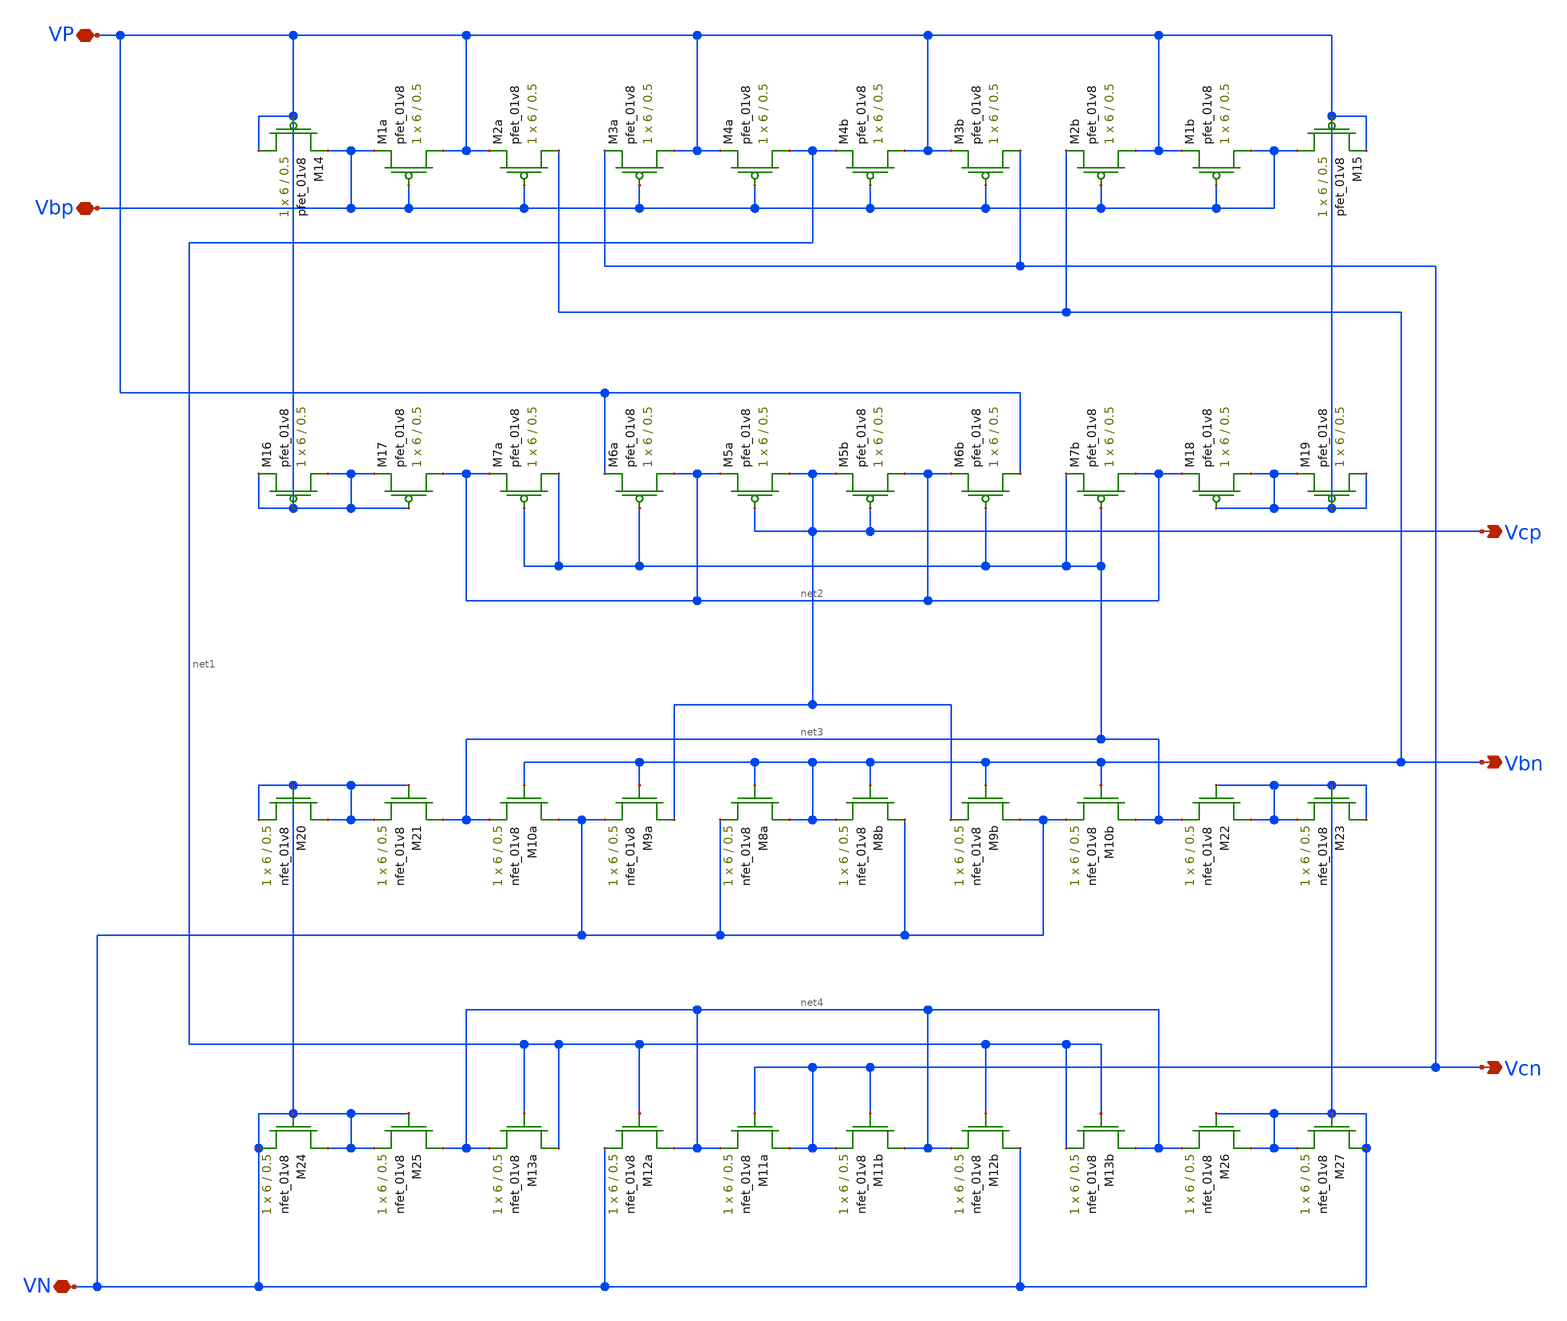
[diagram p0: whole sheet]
** sch_path: schematic/cascode_bias_LDS_old.sch
**.subckt cascode_bias_LDS_old VP VN Vcp Vbn Vcn Vbp
*.iopin VP
*.iopin VN
*.opin Vcp
*.opin Vbn
*.opin Vcn
*.iopin Vbp
XM1a VP Vbp Vbp VDD sky130_fd_pr__pfet_01v8 L=0.5 W=6 nf=1 ad='int((nf+1)/2) * W/nf * 0.29' as='int((nf+2)/2) * W/nf * 0.29'
+ pd='2*int((nf+1)/2) * (W/nf + 0.29)' ps='2*int((nf+2)/2) * (W/nf + 0.29)' nrd='0.29 / W' nrs='0.29 / W'
+ sa=0 sb=0 sd=0 mult=1 m=1
XM2a Vbn Vbp VP VDD sky130_fd_pr__pfet_01v8 L=0.5 W=6 nf=1 ad='int((nf+1)/2) * W/nf * 0.29' as='int((nf+2)/2) * W/nf * 0.29'
+ pd='2*int((nf+1)/2) * (W/nf + 0.29)' ps='2*int((nf+2)/2) * (W/nf + 0.29)' nrd='0.29 / W' nrs='0.29 / W'
+ sa=0 sb=0 sd=0 mult=1 m=1
XM3a VP Vbp Vcn VDD sky130_fd_pr__pfet_01v8 L=0.5 W=6 nf=1 ad='int((nf+1)/2) * W/nf * 0.29' as='int((nf+2)/2) * W/nf * 0.29'
+ pd='2*int((nf+1)/2) * (W/nf + 0.29)' ps='2*int((nf+2)/2) * (W/nf + 0.29)' nrd='0.29 / W' nrs='0.29 / W'
+ sa=0 sb=0 sd=0 mult=1 m=1
XM4a net1 Vbp VP VDD sky130_fd_pr__pfet_01v8 L=0.5 W=6 nf=1 ad='int((nf+1)/2) * W/nf * 0.29' as='int((nf+2)/2) * W/nf * 0.29'
+ pd='2*int((nf+1)/2) * (W/nf + 0.29)' ps='2*int((nf+2)/2) * (W/nf + 0.29)' nrd='0.29 / W' nrs='0.29 / W'
+ sa=0 sb=0 sd=0 mult=1 m=1
XM4b VP Vbp net1 VDD sky130_fd_pr__pfet_01v8 L=0.5 W=6 nf=1 ad='int((nf+1)/2) * W/nf * 0.29' as='int((nf+2)/2) * W/nf * 0.29'
+ pd='2*int((nf+1)/2) * (W/nf + 0.29)' ps='2*int((nf+2)/2) * (W/nf + 0.29)' nrd='0.29 / W' nrs='0.29 / W'
+ sa=0 sb=0 sd=0 mult=1 m=1
XM3b Vcn Vbp VP VDD sky130_fd_pr__pfet_01v8 L=0.5 W=6 nf=1 ad='int((nf+1)/2) * W/nf * 0.29' as='int((nf+2)/2) * W/nf * 0.29'
+ pd='2*int((nf+1)/2) * (W/nf + 0.29)' ps='2*int((nf+2)/2) * (W/nf + 0.29)' nrd='0.29 / W' nrs='0.29 / W'
+ sa=0 sb=0 sd=0 mult=1 m=1
XM2b VP Vbp Vbn VDD sky130_fd_pr__pfet_01v8 L=0.5 W=6 nf=1 ad='int((nf+1)/2) * W/nf * 0.29' as='int((nf+2)/2) * W/nf * 0.29'
+ pd='2*int((nf+1)/2) * (W/nf + 0.29)' ps='2*int((nf+2)/2) * (W/nf + 0.29)' nrd='0.29 / W' nrs='0.29 / W'
+ sa=0 sb=0 sd=0 mult=1 m=1
XM1b Vbp Vbp VP VDD sky130_fd_pr__pfet_01v8 L=0.5 W=6 nf=1 ad='int((nf+1)/2) * W/nf * 0.29' as='int((nf+2)/2) * W/nf * 0.29'
+ pd='2*int((nf+1)/2) * (W/nf + 0.29)' ps='2*int((nf+2)/2) * (W/nf + 0.29)' nrd='0.29 / W' nrs='0.29 / W'
+ sa=0 sb=0 sd=0 mult=1 m=1
XM7a net3 net3 net2 VDD sky130_fd_pr__pfet_01v8 L=0.5 W=6 nf=1 ad='int((nf+1)/2) * W/nf * 0.29' as='int((nf+2)/2) * W/nf * 0.29'
+ pd='2*int((nf+1)/2) * (W/nf + 0.29)' ps='2*int((nf+2)/2) * (W/nf + 0.29)' nrd='0.29 / W' nrs='0.29 / W'
+ sa=0 sb=0 sd=0 mult=1 m=1
XM6a net2 net3 VP VDD sky130_fd_pr__pfet_01v8 L=0.5 W=6 nf=1 ad='int((nf+1)/2) * W/nf * 0.29' as='int((nf+2)/2) * W/nf * 0.29'
+ pd='2*int((nf+1)/2) * (W/nf + 0.29)' ps='2*int((nf+2)/2) * (W/nf + 0.29)' nrd='0.29 / W' nrs='0.29 / W'
+ sa=0 sb=0 sd=0 mult=1 m=1
XM5a Vcp Vcp net2 VDD sky130_fd_pr__pfet_01v8 L=0.5 W=6 nf=1 ad='int((nf+1)/2) * W/nf * 0.29' as='int((nf+2)/2) * W/nf * 0.29'
+ pd='2*int((nf+1)/2) * (W/nf + 0.29)' ps='2*int((nf+2)/2) * (W/nf + 0.29)' nrd='0.29 / W' nrs='0.29 / W'
+ sa=0 sb=0 sd=0 mult=1 m=1
XM5b net2 Vcp Vcp VDD sky130_fd_pr__pfet_01v8 L=0.5 W=6 nf=1 ad='int((nf+1)/2) * W/nf * 0.29' as='int((nf+2)/2) * W/nf * 0.29'
+ pd='2*int((nf+1)/2) * (W/nf + 0.29)' ps='2*int((nf+2)/2) * (W/nf + 0.29)' nrd='0.29 / W' nrs='0.29 / W'
+ sa=0 sb=0 sd=0 mult=1 m=1
XM6b VP net3 net2 VDD sky130_fd_pr__pfet_01v8 L=0.5 W=6 nf=1 ad='int((nf+1)/2) * W/nf * 0.29' as='int((nf+2)/2) * W/nf * 0.29'
+ pd='2*int((nf+1)/2) * (W/nf + 0.29)' ps='2*int((nf+2)/2) * (W/nf + 0.29)' nrd='0.29 / W' nrs='0.29 / W'
+ sa=0 sb=0 sd=0 mult=1 m=1
XM7b net2 net3 net3 VDD sky130_fd_pr__pfet_01v8 L=0.5 W=6 nf=1 ad='int((nf+1)/2) * W/nf * 0.29' as='int((nf+2)/2) * W/nf * 0.29'
+ pd='2*int((nf+1)/2) * (W/nf + 0.29)' ps='2*int((nf+2)/2) * (W/nf + 0.29)' nrd='0.29 / W' nrs='0.29 / W'
+ sa=0 sb=0 sd=0 mult=1 m=1
XM8a Vbn Vbn VN GND sky130_fd_pr__nfet_01v8 L=0.5 W=6 nf=1 ad='int((nf+1)/2) * W/nf * 0.29' as='int((nf+2)/2) * W/nf * 0.29'
+ pd='2*int((nf+1)/2) * (W/nf + 0.29)' ps='2*int((nf+2)/2) * (W/nf + 0.29)' nrd='0.29 / W' nrs='0.29 / W'
+ sa=0 sb=0 sd=0 mult=1 m=1
XM8b VN Vbn Vbn GND sky130_fd_pr__nfet_01v8 L=0.5 W=6 nf=1 ad='int((nf+1)/2) * W/nf * 0.29' as='int((nf+2)/2) * W/nf * 0.29'
+ pd='2*int((nf+1)/2) * (W/nf + 0.29)' ps='2*int((nf+2)/2) * (W/nf + 0.29)' nrd='0.29 / W' nrs='0.29 / W'
+ sa=0 sb=0 sd=0 mult=1 m=1
XM10a VN Vbn net3 GND sky130_fd_pr__nfet_01v8 L=0.5 W=6 nf=1 ad='int((nf+1)/2) * W/nf * 0.29' as='int((nf+2)/2) * W/nf * 0.29'
+ pd='2*int((nf+1)/2) * (W/nf + 0.29)' ps='2*int((nf+2)/2) * (W/nf + 0.29)' nrd='0.29 / W' nrs='0.29 / W'
+ sa=0 sb=0 sd=0 mult=1 m=1
XM9a Vcp Vbn VN GND sky130_fd_pr__nfet_01v8 L=0.5 W=6 nf=1 ad='int((nf+1)/2) * W/nf * 0.29' as='int((nf+2)/2) * W/nf * 0.29'
+ pd='2*int((nf+1)/2) * (W/nf + 0.29)' ps='2*int((nf+2)/2) * (W/nf + 0.29)' nrd='0.29 / W' nrs='0.29 / W'
+ sa=0 sb=0 sd=0 mult=1 m=1
XM9b VN Vbn Vcp GND sky130_fd_pr__nfet_01v8 L=0.5 W=6 nf=1 ad='int((nf+1)/2) * W/nf * 0.29' as='int((nf+2)/2) * W/nf * 0.29'
+ pd='2*int((nf+1)/2) * (W/nf + 0.29)' ps='2*int((nf+2)/2) * (W/nf + 0.29)' nrd='0.29 / W' nrs='0.29 / W'
+ sa=0 sb=0 sd=0 mult=1 m=1
XM10b net3 Vbn VN GND sky130_fd_pr__nfet_01v8 L=0.5 W=6 nf=1 ad='int((nf+1)/2) * W/nf * 0.29' as='int((nf+2)/2) * W/nf * 0.29'
+ pd='2*int((nf+1)/2) * (W/nf + 0.29)' ps='2*int((nf+2)/2) * (W/nf + 0.29)' nrd='0.29 / W' nrs='0.29 / W'
+ sa=0 sb=0 sd=0 mult=1 m=1
XM11a Vcn Vcn net4 GND sky130_fd_pr__nfet_01v8 L=0.5 W=6 nf=1 ad='int((nf+1)/2) * W/nf * 0.29' as='int((nf+2)/2) * W/nf * 0.29'
+ pd='2*int((nf+1)/2) * (W/nf + 0.29)' ps='2*int((nf+2)/2) * (W/nf + 0.29)' nrd='0.29 / W' nrs='0.29 / W'
+ sa=0 sb=0 sd=0 mult=1 m=1
XM11b net4 Vcn Vcn GND sky130_fd_pr__nfet_01v8 L=0.5 W=6 nf=1 ad='int((nf+1)/2) * W/nf * 0.29' as='int((nf+2)/2) * W/nf * 0.29'
+ pd='2*int((nf+1)/2) * (W/nf + 0.29)' ps='2*int((nf+2)/2) * (W/nf + 0.29)' nrd='0.29 / W' nrs='0.29 / W'
+ sa=0 sb=0 sd=0 mult=1 m=1
XM13a net1 net1 net4 GND sky130_fd_pr__nfet_01v8 L=0.5 W=6 nf=1 ad='int((nf+1)/2) * W/nf * 0.29' as='int((nf+2)/2) * W/nf * 0.29'
+ pd='2*int((nf+1)/2) * (W/nf + 0.29)' ps='2*int((nf+2)/2) * (W/nf + 0.29)' nrd='0.29 / W' nrs='0.29 / W'
+ sa=0 sb=0 sd=0 mult=1 m=1
XM12a net4 net1 VN GND sky130_fd_pr__nfet_01v8 L=0.5 W=6 nf=1 ad='int((nf+1)/2) * W/nf * 0.29' as='int((nf+2)/2) * W/nf * 0.29'
+ pd='2*int((nf+1)/2) * (W/nf + 0.29)' ps='2*int((nf+2)/2) * (W/nf + 0.29)' nrd='0.29 / W' nrs='0.29 / W'
+ sa=0 sb=0 sd=0 mult=1 m=1
XM12b VN net1 net4 GND sky130_fd_pr__nfet_01v8 L=0.5 W=6 nf=1 ad='int((nf+1)/2) * W/nf * 0.29' as='int((nf+2)/2) * W/nf * 0.29'
+ pd='2*int((nf+1)/2) * (W/nf + 0.29)' ps='2*int((nf+2)/2) * (W/nf + 0.29)' nrd='0.29 / W' nrs='0.29 / W'
+ sa=0 sb=0 sd=0 mult=1 m=1
XM13b net4 net1 net1 GND sky130_fd_pr__nfet_01v8 L=0.5 W=6 nf=1 ad='int((nf+1)/2) * W/nf * 0.29' as='int((nf+2)/2) * W/nf * 0.29'
+ pd='2*int((nf+1)/2) * (W/nf + 0.29)' ps='2*int((nf+2)/2) * (W/nf + 0.29)' nrd='0.29 / W' nrs='0.29 / W'
+ sa=0 sb=0 sd=0 mult=1 m=1
XM15 Vbp VP VP VDD sky130_fd_pr__pfet_01v8 L=0.5 W=6 nf=1 ad='int((nf+1)/2) * W/nf * 0.29' as='int((nf+2)/2) * W/nf * 0.29'
+ pd='2*int((nf+1)/2) * (W/nf + 0.29)' ps='2*int((nf+2)/2) * (W/nf + 0.29)' nrd='0.29 / W' nrs='0.29 / W'
+ sa=0 sb=0 sd=0 mult=1 m=1
XM25 net4 VN VN GND sky130_fd_pr__nfet_01v8 L=0.5 W=6 nf=1 ad='int((nf+1)/2) * W/nf * 0.29' as='int((nf+2)/2) * W/nf * 0.29'
+ pd='2*int((nf+1)/2) * (W/nf + 0.29)' ps='2*int((nf+2)/2) * (W/nf + 0.29)' nrd='0.29 / W' nrs='0.29 / W'
+ sa=0 sb=0 sd=0 mult=1 m=1
XM24 VN VN VN GND sky130_fd_pr__nfet_01v8 L=0.5 W=6 nf=1 ad='int((nf+1)/2) * W/nf * 0.29' as='int((nf+2)/2) * W/nf * 0.29'
+ pd='2*int((nf+1)/2) * (W/nf + 0.29)' ps='2*int((nf+2)/2) * (W/nf + 0.29)' nrd='0.29 / W' nrs='0.29 / W'
+ sa=0 sb=0 sd=0 mult=1 m=1
XM26 VN VN net4 GND sky130_fd_pr__nfet_01v8 L=0.5 W=6 nf=1 ad='int((nf+1)/2) * W/nf * 0.29' as='int((nf+2)/2) * W/nf * 0.29'
+ pd='2*int((nf+1)/2) * (W/nf + 0.29)' ps='2*int((nf+2)/2) * (W/nf + 0.29)' nrd='0.29 / W' nrs='0.29 / W'
+ sa=0 sb=0 sd=0 mult=1 m=1
XM27 VN VN VN GND sky130_fd_pr__nfet_01v8 L=0.5 W=6 nf=1 ad='int((nf+1)/2) * W/nf * 0.29' as='int((nf+2)/2) * W/nf * 0.29'
+ pd='2*int((nf+1)/2) * (W/nf + 0.29)' ps='2*int((nf+2)/2) * (W/nf + 0.29)' nrd='0.29 / W' nrs='0.29 / W'
+ sa=0 sb=0 sd=0 mult=1 m=1
XM21 net3 VN VN GND sky130_fd_pr__nfet_01v8 L=0.5 W=6 nf=1 ad='int((nf+1)/2) * W/nf * 0.29' as='int((nf+2)/2) * W/nf * 0.29'
+ pd='2*int((nf+1)/2) * (W/nf + 0.29)' ps='2*int((nf+2)/2) * (W/nf + 0.29)' nrd='0.29 / W' nrs='0.29 / W'
+ sa=0 sb=0 sd=0 mult=1 m=1
XM20 VN VN VN GND sky130_fd_pr__nfet_01v8 L=0.5 W=6 nf=1 ad='int((nf+1)/2) * W/nf * 0.29' as='int((nf+2)/2) * W/nf * 0.29'
+ pd='2*int((nf+1)/2) * (W/nf + 0.29)' ps='2*int((nf+2)/2) * (W/nf + 0.29)' nrd='0.29 / W' nrs='0.29 / W'
+ sa=0 sb=0 sd=0 mult=1 m=1
XM23 VN VN VN GND sky130_fd_pr__nfet_01v8 L=0.5 W=6 nf=1 ad='int((nf+1)/2) * W/nf * 0.29' as='int((nf+2)/2) * W/nf * 0.29'
+ pd='2*int((nf+1)/2) * (W/nf + 0.29)' ps='2*int((nf+2)/2) * (W/nf + 0.29)' nrd='0.29 / W' nrs='0.29 / W'
+ sa=0 sb=0 sd=0 mult=1 m=1
XM22 VN VN net3 GND sky130_fd_pr__nfet_01v8 L=0.5 W=6 nf=1 ad='int((nf+1)/2) * W/nf * 0.29' as='int((nf+2)/2) * W/nf * 0.29'
+ pd='2*int((nf+1)/2) * (W/nf + 0.29)' ps='2*int((nf+2)/2) * (W/nf + 0.29)' nrd='0.29 / W' nrs='0.29 / W'
+ sa=0 sb=0 sd=0 mult=1 m=1
XM14 VP VP Vbp VDD sky130_fd_pr__pfet_01v8 L=0.5 W=6 nf=1 ad='int((nf+1)/2) * W/nf * 0.29' as='int((nf+2)/2) * W/nf * 0.29'
+ pd='2*int((nf+1)/2) * (W/nf + 0.29)' ps='2*int((nf+2)/2) * (W/nf + 0.29)' nrd='0.29 / W' nrs='0.29 / W'
+ sa=0 sb=0 sd=0 mult=1 m=1
XM17 net2 VP VP VDD sky130_fd_pr__pfet_01v8 L=0.5 W=6 nf=1 ad='int((nf+1)/2) * W/nf * 0.29' as='int((nf+2)/2) * W/nf * 0.29'
+ pd='2*int((nf+1)/2) * (W/nf + 0.29)' ps='2*int((nf+2)/2) * (W/nf + 0.29)' nrd='0.29 / W' nrs='0.29 / W'
+ sa=0 sb=0 sd=0 mult=1 m=1
XM16 VP VP VP VDD sky130_fd_pr__pfet_01v8 L=0.5 W=6 nf=1 ad='int((nf+1)/2) * W/nf * 0.29' as='int((nf+2)/2) * W/nf * 0.29'
+ pd='2*int((nf+1)/2) * (W/nf + 0.29)' ps='2*int((nf+2)/2) * (W/nf + 0.29)' nrd='0.29 / W' nrs='0.29 / W'
+ sa=0 sb=0 sd=0 mult=1 m=1
XM18 VP VP net2 VDD sky130_fd_pr__pfet_01v8 L=0.5 W=6 nf=1 ad='int((nf+1)/2) * W/nf * 0.29' as='int((nf+2)/2) * W/nf * 0.29'
+ pd='2*int((nf+1)/2) * (W/nf + 0.29)' ps='2*int((nf+2)/2) * (W/nf + 0.29)' nrd='0.29 / W' nrs='0.29 / W'
+ sa=0 sb=0 sd=0 mult=1 m=1
XM19 VP VP VP VDD sky130_fd_pr__pfet_01v8 L=0.5 W=6 nf=1 ad='int((nf+1)/2) * W/nf * 0.29' as='int((nf+2)/2) * W/nf * 0.29'
+ pd='2*int((nf+1)/2) * (W/nf + 0.29)' ps='2*int((nf+2)/2) * (W/nf + 0.29)' nrd='0.29 / W' nrs='0.29 / W'
+ sa=0 sb=0 sd=0 mult=1 m=1
**.ends
.end
